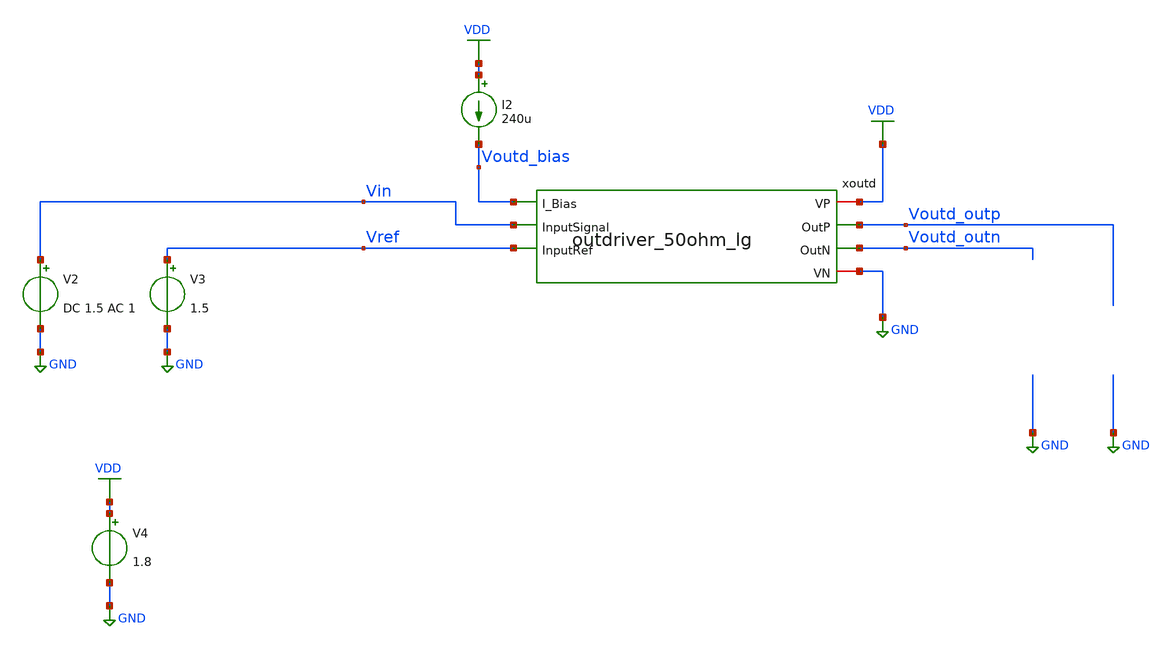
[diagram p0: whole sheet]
** sch_path: xschem/test/test_outd.sch
**.subckt test_outd
I2 VDD Voutd_bias 240u
V2 Vin GND DC 1.5 AC 1
V3 Vref GND 1.5
V4 VDD GND 1.8
xoutd VDD Voutd_outp Voutd_outn Voutd_bias Vin Vref GND outdriver_50ohm_lg
**** begin user architecture code


*.options savecurrents
.option warn=1
.control
set wr_vecnames
set wr_singlescale
set hcopydevtype=svg

reset

save all
op
save currents
write test_outd.raw
run
reset
save all
ac dec 10 1 1T
plot db(v(voutd_outp)-v(voutd_outn))
plot db(v(xoutd.V_da3_P)-v(xoutd.V_da3_N))
plot db(v(xoutd.V_da2_P)-v(xoutd.V_da2_N))
plot db(v(xoutd.V_da1_P)-v(xoutd.V_da1_N))

* hardcopy filter_gain.svg db(v(Vfilt1_N)-v(Vfilt1_P))
* noise v(voutd_outp) v2 dec 1000 2MEG 2G
* print all
* * wrdata result_noise.csv inoise_total onoise_total
* setplot noise1
* plot inoise_spectrum
* plot onoise_spectrum

reset
* noise v(xoutd.v_da1_p) v2 dec 1000 2MEG 2G
* setplot noise1
* plot inoise_spectrum
* plot onoise_spectrum
* run

* noise v(xoutd.v_da1_p) v2 dec 1000 10 1T
* print all
* setplot noise3
* plot inoise_spectrum
* plot onoise_spectrum
* run

* noise v(V_da2_P) v2 dec 1000 2MEG 2G
* setplot noise5
* plot inoise_spectrum
* plot onoise_spectrum
* run


noise v(voutd_outp, voutd_outn) v2 dec 100 10 1T
print all
setplot noise1
plot inoise_spectrum
plot onoise_spectrum
run

noise v(voutd_outp, voutd_outn) v2 dec 100 1MEG 10G
print all
setplot noise3
plot inoise_spectrum
plot onoise_spectrum
run




* noise v(V_da2_P) v2 dec 1000 10 1T
* print all
* setplot noise11
* plot inoise_spectrum
* plot onoise_spectrum
* run



.endc




* .include ../../tia.spice
* .include ../../filter_diff.spice
* .include ../../cmm_sense3.spice

* .include tia.spice
* .include filter_diff.spice
* .include diffamp.spice
* .include cmm_sense3.spice
* .include comp.spice
.include outdriver_50ohm_lg.spice
*.include outdriver_cascode.spice



* .lib $::SKYWATER_MODELS/sky130.lib.spice #model#
.lib $::SKYWATER_MODELS/sky130.lib.spice.tt.red tt
* .lib /home/simon/share/pdk/sky130A/libs.tech/ngspice/sky130.lib.spice.tt.red tt

**** end user architecture code
**.ends

* expanding   symbol:
*+  /home/simon/code/hibpm-sky130a-tapeout/xschem/outdriver/outdriver_50ohm_lg.sym # of pins=7
** sym_path: xschem/outdriver/outdriver_50ohm_lg.sym
** sch_path: xschem/outdriver/outdriver_50ohm_lg.sch
.subckt outdriver_50ohm_lg VP OutP OutN I_Bias InputSignal InputRef VN
*.iopin VN
*.ipin InputRef
*.iopin VP
*.ipin I_Bias
*.ipin InputSignal
*.opin OutN
*.opin OutP
XM17 net1 VM18D VN VN sky130_fd_pr__nfet_01v8_lvt L=0.3 W=2 nf=1 ad='int((nf+1)/2) * W/nf * 0.29' as='int((nf+2)/2) * W/nf * 0.29'
+ pd='2*int((nf+1)/2) * (W/nf + 0.29)' ps='2*int((nf+2)/2) * (W/nf + 0.29)' nrd='0.29 / W' nrs='0.29 / W'
+ sa=0 sb=0 sd=0 mult=6 m=6
XM18 VM18D VM18D net1 VN sky130_fd_pr__nfet_01v8_lvt L=0.15 W=2 nf=1 ad='int((nf+1)/2) * W/nf * 0.29'
+ as='int((nf+2)/2) * W/nf * 0.29' pd='2*int((nf+1)/2) * (W/nf + 0.29)' ps='2*int((nf+2)/2) * (W/nf + 0.29)'
+ nrd='0.29 / W' nrs='0.29 / W' sa=0 sb=0 sd=0 mult=12 m=12
XM7 I_Bias I_Bias VM18D VM18D sky130_fd_pr__nfet_01v8_lvt L=0.15 W=2 nf=1 ad='int((nf+1)/2) * W/nf * 0.29'
+ as='int((nf+2)/2) * W/nf * 0.29' pd='2*int((nf+1)/2) * (W/nf + 0.29)' ps='2*int((nf+2)/2) * (W/nf + 0.29)'
+ nrd='0.29 / W' nrs='0.29 / W' sa=0 sb=0 sd=0 mult=20 m=20
XM5 VM5D net2 net3 VN sky130_fd_pr__nfet_01v8_lvt L=0.15 W=2 nf=1 ad='int((nf+1)/2) * W/nf * 0.29' as='int((nf+2)/2) * W/nf * 0.29'
+ pd='2*int((nf+1)/2) * (W/nf + 0.29)' ps='2*int((nf+2)/2) * (W/nf + 0.29)' nrd='0.29 / W' nrs='0.29 / W'
+ sa=0 sb=0 sd=0 mult=12*5 m=12*5
XM8 net3 net2 VN VN sky130_fd_pr__nfet_01v8_lvt L=0.3 W=2 nf=1 ad='int((nf+1)/2) * W/nf * 0.29' as='int((nf+2)/2) * W/nf * 0.29'
+ pd='2*int((nf+1)/2) * (W/nf + 0.29)' ps='2*int((nf+2)/2) * (W/nf + 0.29)' nrd='0.29 / W' nrs='0.29 / W'
+ sa=0 sb=0 sd=0 mult=6*5 m=6*5
XM6 net2 I_Bias VM18D VM18D sky130_fd_pr__nfet_01v8_lvt L=8 W=1 nf=1 ad='int((nf+1)/2) * W/nf * 0.29'
+ as='int((nf+2)/2) * W/nf * 0.29' pd='2*int((nf+1)/2) * (W/nf + 0.29)' ps='2*int((nf+2)/2) * (W/nf + 0.29)'
+ nrd='0.29 / W' nrs='0.29 / W' sa=0 sb=0 sd=0 mult=1 m=1
XC1 VN VP sky130_fd_pr__cap_mim_m3_1 W=15 L=30 MF=1 m=1
XM15 VM15D net2 net4 VN sky130_fd_pr__nfet_01v8_lvt L=0.15 W=2 nf=1 ad='int((nf+1)/2) * W/nf * 0.29'
+ as='int((nf+2)/2) * W/nf * 0.29' pd='2*int((nf+1)/2) * (W/nf + 0.29)' ps='2*int((nf+2)/2) * (W/nf + 0.29)'
+ nrd='0.29 / W' nrs='0.29 / W' sa=0 sb=0 sd=0 mult=34*12 m=34*12
XM16 net4 net2 VN VN sky130_fd_pr__nfet_01v8_lvt L=0.3 W=2 nf=1 ad='int((nf+1)/2) * W/nf * 0.29' as='int((nf+2)/2) * W/nf * 0.29'
+ pd='2*int((nf+1)/2) * (W/nf + 0.29)' ps='2*int((nf+2)/2) * (W/nf + 0.29)' nrd='0.29 / W' nrs='0.29 / W'
+ sa=0 sb=0 sd=0 mult=34*6 m=34*6
XM4 OutP V_da2_N VM15D VN sky130_fd_pr__nfet_01v8_lvt L=0.15 W=2 nf=1 ad='int((nf+1)/2) * W/nf * 0.29'
+ as='int((nf+2)/2) * W/nf * 0.29' pd='2*int((nf+1)/2) * (W/nf + 0.29)' ps='2*int((nf+2)/2) * (W/nf + 0.29)'
+ nrd='0.29 / W' nrs='0.29 / W' sa=0 sb=0 sd=0 mult=30 m=30
XM23 V_da2_P InputSignal VM5D VN sky130_fd_pr__nfet_01v8_lvt L=0.15 W=2 nf=1 ad='int((nf+1)/2) * W/nf * 0.29'
+ as='int((nf+2)/2) * W/nf * 0.29' pd='2*int((nf+1)/2) * (W/nf + 0.29)' ps='2*int((nf+2)/2) * (W/nf + 0.29)'
+ nrd='0.29 / W' nrs='0.29 / W' sa=0 sb=0 sd=0 mult=6 m=6
XM19 OutN V_da2_P VM15D VN sky130_fd_pr__nfet_01v8_lvt L=0.15 W=2 nf=1 ad='int((nf+1)/2) * W/nf * 0.29'
+ as='int((nf+2)/2) * W/nf * 0.29' pd='2*int((nf+1)/2) * (W/nf + 0.29)' ps='2*int((nf+2)/2) * (W/nf + 0.29)'
+ nrd='0.29 / W' nrs='0.29 / W' sa=0 sb=0 sd=0 mult=30 m=30
XM14 V_da2_N InputRef VM5D VN sky130_fd_pr__nfet_01v8_lvt L=0.15 W=2 nf=1 ad='int((nf+1)/2) * W/nf * 0.29'
+ as='int((nf+2)/2) * W/nf * 0.29' pd='2*int((nf+1)/2) * (W/nf + 0.29)' ps='2*int((nf+2)/2) * (W/nf + 0.29)'
+ nrd='0.29 / W' nrs='0.29 / W' sa=0 sb=0 sd=0 mult=6 m=6
XR12 OutP VP VN sky130_fd_pr__res_high_po_1p41 L=4 mult=22 m=22
XR13 OutN VP VN sky130_fd_pr__res_high_po_1p41 L=4 mult=22 m=22
XR1 V_da2_P VP VN sky130_fd_pr__res_xhigh_po_1p41 L=2 mult=2*4 m=2*4
XR15 V_da2_N VP VN sky130_fd_pr__res_xhigh_po_1p41 L=2 mult=2*4 m=2*4
XC6 VN InputRef sky130_fd_pr__cap_mim_m3_1 W=10 L=6 MF=1 m=1
XC2 VN VP sky130_fd_pr__cap_mim_m3_1 W=15 L=30 MF=1 m=1
XC4 VN VP sky130_fd_pr__cap_mim_m3_1 W=15 L=30 MF=1 m=1
XC3 VN net2 sky130_fd_pr__cap_mim_m3_1 W=10 L=16 MF=1 m=1
.ends

.GLOBAL GND
.GLOBAL VDD
.end
